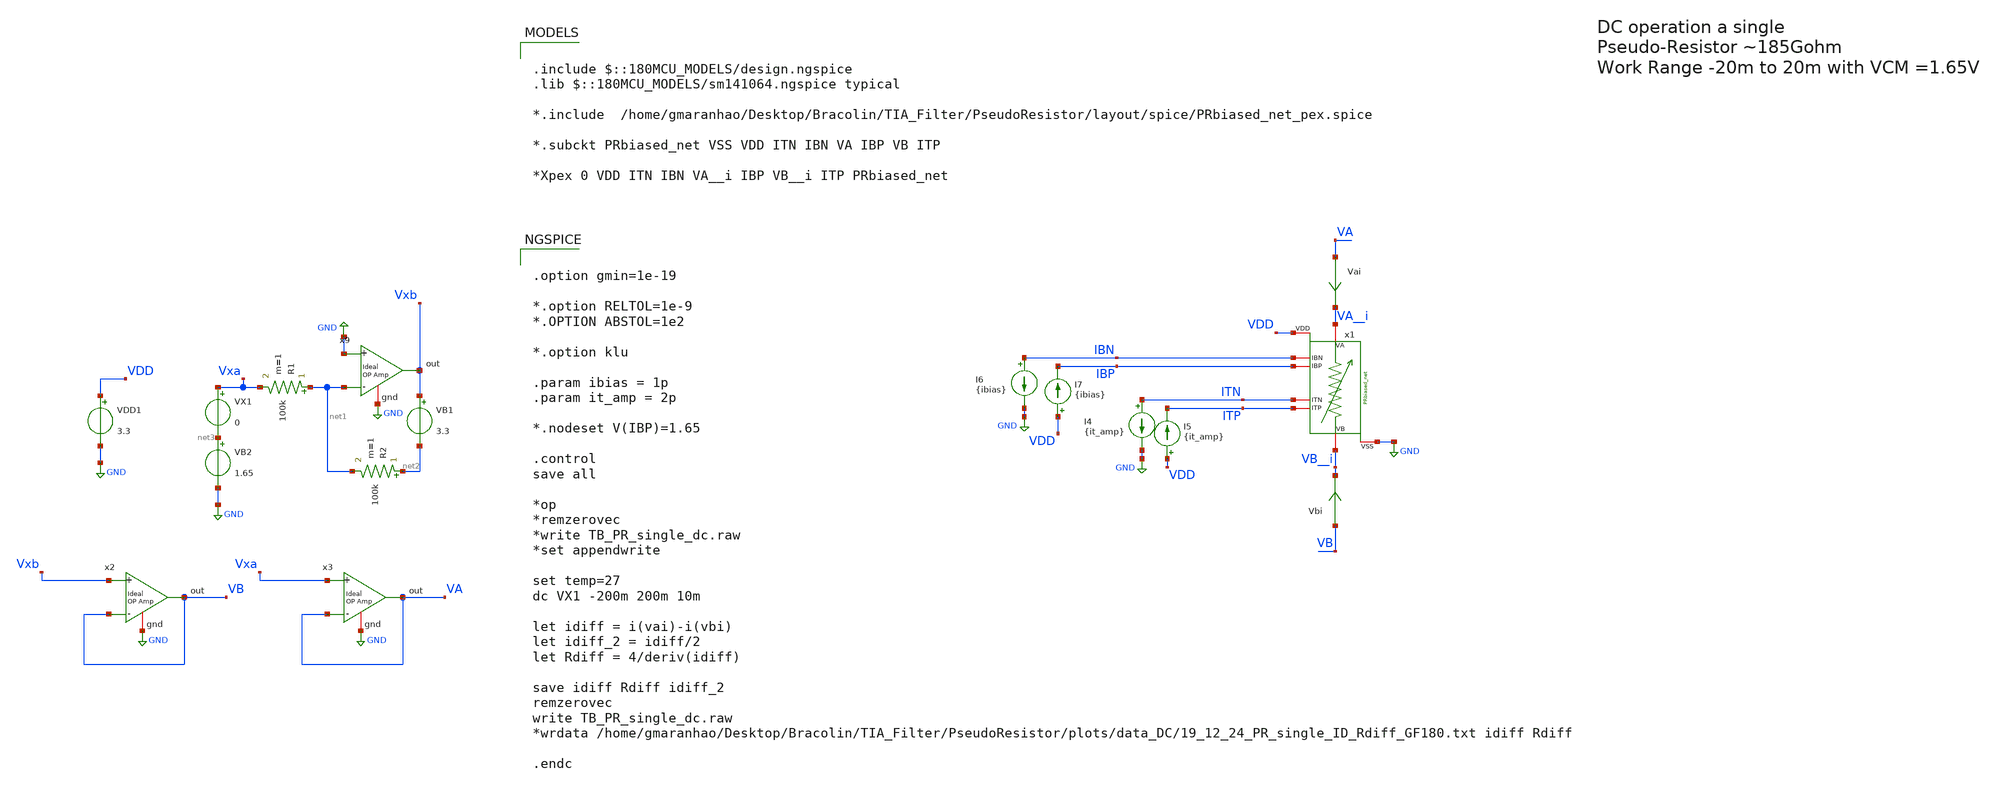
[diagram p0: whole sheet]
** sch_path: TIA_Filter/PseudoResistor/TB_PR_single_dc.sch
**.subckt TB_PR_single_dc
I4 ITN GND {it_amp}
I5 VDD ITP {it_amp}
I6 IBN GND {ibias}
I7 VDD IBP {ibias}
Vai VA VA__i 0
.save i(vai)
Vbi VB VB__i 0
.save i(vbi)
VDD1 VDD GND 3.3
VX1 Vxa net3 0
VB1 Vxb net2 3.3
R1 net1 Vxa 100k m=1
R2 net2 net1 100k m=1
VB2 net3 GND 1.65
x2 VB Vxb VB GND ampOp_ideal
x3 VA Vxa VA GND ampOp_ideal
x9 Vxb GND net1 GND ampOp_ideal
x1 VA__i VB__i IBN IBP ITN ITP VDD GND PRbiased_net
**** begin user architecture code

.include $::180MCU_MODELS/design.ngspice
.lib $::180MCU_MODELS/sm141064.ngspice typical

*.include  /home/gmaranhao/Desktop/Bracolin/TIA_Filter/PseudoResistor/layout/spice/PRbiased_net_pex.spice

*.subckt PRbiased_net VSS VDD ITN IBN VA IBP VB ITP

*Xpex 0 VDD ITN IBN VA__i IBP VB__i ITP PRbiased_net




.option gmin=1e-19

*.option RELTOL=1e-9
*.OPTION ABSTOL=1e2

*.option klu

.param ibias = 1p
.param it_amp = 2p

*.nodeset V(IBP)=1.65

.control
save all

*op
*remzerovec
*write TB_PR_single_dc.raw
*set appendwrite

set temp=27
dc VX1 -200m 200m 10m

let idiff = i(vai)-i(vbi)
let idiff_2 = idiff/2
let Rdiff = 4/deriv(idiff)

save idiff Rdiff idiff_2
remzerovec
write TB_PR_single_dc.raw
*wrdata
*+ /home/gmaranhao/Desktop/Bracolin/TIA_Filter/PseudoResistor/plots/data_DC/19_12_24_PR_single_ID_Rdiff_GF180.txt idiff Rdiff

.endc


**** end user architecture code
**.ends
.GLOBAL GND
.end
